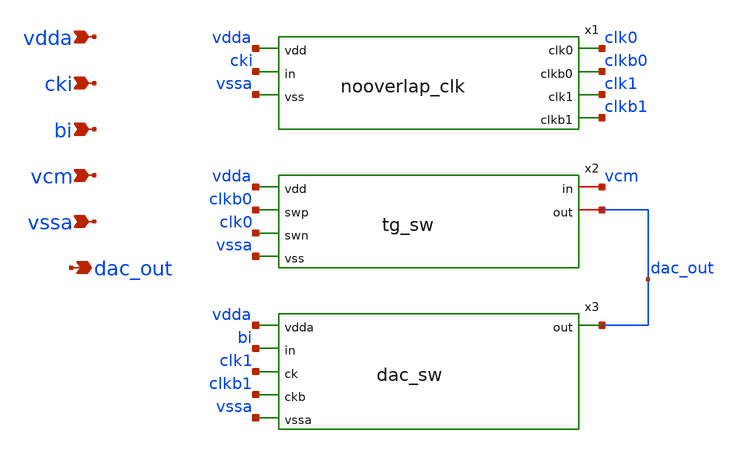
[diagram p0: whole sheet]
** sch_path: xschem/schematics/cdac_sw.sch
**.subckt cdac_sw vdda cki bi vcm vssa dac_out
*.ipin vdda
*.ipin cki
*.ipin bi
*.ipin vcm
*.ipin vssa
*.opin dac_out
x1 vdda cki vssa clk0 clkb0 clk1 clkb1 nooverlap_clk
x2 vdda clkb0 clk0 vssa vcm dac_out tg_sw
x3 vdda bi clk1 clkb1 vssa dac_out dac_sw
**.ends

* expanding   symbol:  nooverlap_clk.sym # of pins=7
** sym_path: xschem/nooverlap_clk.sym
** sch_path: xschem/nooverlap_clk.sch
.subckt nooverlap_clk vdd in vss clk0 clkb0 clk1 clkb1
*.ipin vdd
*.ipin in
*.ipin vss
*.opin clk0
*.opin clkb0
*.opin clk1
*.opin clkb1
x1 in a vss vss vdd vdd net9 sky130_fd_sc_hd__nand2_1
x2 b net1 vss vss vdd vdd net2 sky130_fd_sc_hd__nand2_1
x3 in vss vss vdd vdd net1 sky130_fd_sc_hd__inv_1
x4 net9 vss vss vdd vdd net8 sky130_fd_sc_hd__inv_1
x5 net2 vss vss vdd vdd net3 sky130_fd_sc_hd__inv_1
x6 net8 vss vss vdd vdd net7 sky130_fd_sc_hd__inv_1
x7 net3 vss vss vdd vdd net4 sky130_fd_sc_hd__inv_1
x8 net7 vss vss vdd vdd net6 sky130_fd_sc_hd__inv_4
x9 net4 vss vss vdd vdd net5 sky130_fd_sc_hd__inv_4
x10 net10 vss vss vdd vdd clkb0 sky130_fd_sc_hd__inv_8
x11 net11 vss vss vdd vdd clkb1 sky130_fd_sc_hd__inv_8
x12 clkb0 vss vss vdd vdd clk0 sky130_fd_sc_hd__inv_8
x13 clkb1 vss vss vdd vdd clk1 sky130_fd_sc_hd__inv_8
x14 net6 vss vss vdd vdd b sky130_fd_sc_hd__inv_8
x15 net5 vss vss vdd vdd a sky130_fd_sc_hd__inv_8
x16 a vss vss vdd vdd net11 sky130_fd_sc_hd__inv_8
x17 b vss vss vdd vdd net10 sky130_fd_sc_hd__inv_8
.ends


* expanding   symbol:  tg_sw.sym # of pins=6
** sym_path: xschem/tg_sw.sym
** sch_path: xschem/tg_sw.sch
.subckt tg_sw vdd swp swn vss in out
*.ipin vdd
*.ipin swp
*.ipin swn
*.ipin vss
*.iopin in
*.iopin out
XM1 in swp out vss sky130_fd_pr__nfet_01v8 L=0.15 W=1 nf=1 ad='int((nf+1)/2) * W/nf * 0.29' as='int((nf+2)/2) * W/nf * 0.29'
+ pd='2*int((nf+1)/2) * (W/nf + 0.29)' ps='2*int((nf+2)/2) * (W/nf + 0.29)' nrd='0.29 / W' nrs='0.29 / W'
+ sa=0 sb=0 sd=0 mult=1 m=1
XM2 in swn out vdd sky130_fd_pr__pfet_01v8 L=0.15 W=1.5 nf=1 ad='int((nf+1)/2) * W/nf * 0.29' as='int((nf+2)/2) * W/nf * 0.29'
+ pd='2*int((nf+1)/2) * (W/nf + 0.29)' ps='2*int((nf+2)/2) * (W/nf + 0.29)' nrd='0.29 / W' nrs='0.29 / W'
+ sa=0 sb=0 sd=0 mult=1 m=1
.ends


* expanding   symbol:  dac_sw.sym # of pins=6
** sym_path: dac_sw.sym
** sch_path: dac_sw.sch
.subckt dac_sw vdda in ck ckb vssa out
*.ipin vdda
*.ipin in
*.ipin ck
*.ipin ckb
*.ipin vssa
*.opin out
XM1 net1 in vdda net3 sky130_fd_pr__pfet_01v8 L=0.15 W=1 nf=1 ad='int((nf+1)/2) * W/nf * 0.29' as='int((nf+2)/2) * W/nf * 0.29'
+ pd='2*int((nf+1)/2) * (W/nf + 0.29)' ps='2*int((nf+2)/2) * (W/nf + 0.29)' nrd='0.29 / W' nrs='0.29 / W'
+ sa=0 sb=0 sd=0 mult=1 m=1
XM2 out ckb net1 net4 sky130_fd_pr__pfet_01v8 L=0.15 W=1 nf=1 ad='int((nf+1)/2) * W/nf * 0.29' as='int((nf+2)/2) * W/nf * 0.29'
+ pd='2*int((nf+1)/2) * (W/nf + 0.29)' ps='2*int((nf+2)/2) * (W/nf + 0.29)' nrd='0.29 / W' nrs='0.29 / W'
+ sa=0 sb=0 sd=0 mult=1 m=1
XM3 out ck net2 net5 sky130_fd_pr__nfet_01v8 L=0.15 W=1 nf=1 ad='int((nf+1)/2) * W/nf * 0.29' as='int((nf+2)/2) * W/nf * 0.29'
+ pd='2*int((nf+1)/2) * (W/nf + 0.29)' ps='2*int((nf+2)/2) * (W/nf + 0.29)' nrd='0.29 / W' nrs='0.29 / W'
+ sa=0 sb=0 sd=0 mult=1 m=1
XM4 net2 in vssa net6 sky130_fd_pr__nfet_01v8 L=0.15 W=1 nf=1 ad='int((nf+1)/2) * W/nf * 0.29' as='int((nf+2)/2) * W/nf * 0.29'
+ pd='2*int((nf+1)/2) * (W/nf + 0.29)' ps='2*int((nf+2)/2) * (W/nf + 0.29)' nrd='0.29 / W' nrs='0.29 / W'
+ sa=0 sb=0 sd=0 mult=1 m=1
.ends

.end
